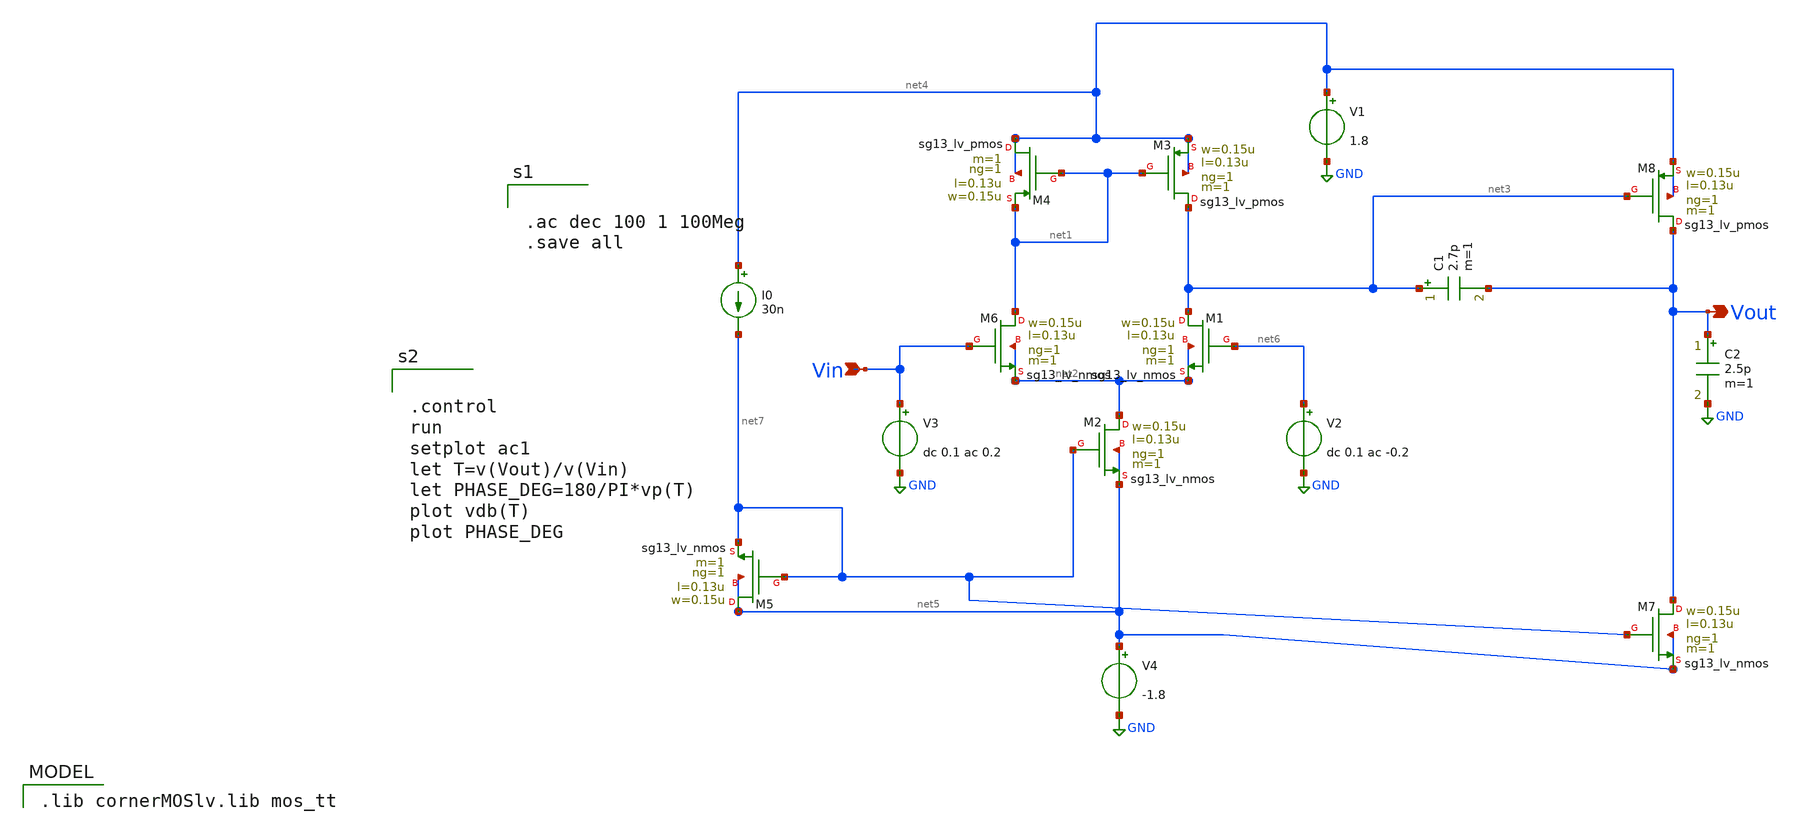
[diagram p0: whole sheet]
** sch_path: twostage.sch
* (c) 2024-2025 H. Pretl, Apache-2.0 license
**.subckt twostage Vout Vin
*.opin Vout
*.ipin Vin
V1 net4 GND 1.8
XM6 net1 Vin net2 net2 sg13_lv_nmos w=0.15u l=0.13u ng=1 m=1 mm_ok=1
XM1 net3 net6 net2 net2 sg13_lv_nmos w=0.15u l=0.13u ng=1 m=1 mm_ok=1
XM2 net2 net7 net5 net5 sg13_lv_nmos w=0.15u l=0.13u ng=1 m=1 mm_ok=1
XM3 net3 net1 net4 net4 sg13_lv_pmos w=0.15u l=0.13u ng=1 m=1 mm_ok=1
XM4 net4 net1 net1 net4 sg13_lv_pmos w=0.15u l=0.13u ng=1 m=1 mm_ok=1
V2 net6 GND dc 0.1 ac -0.2
V3 Vin GND dc 0.1 ac 0.2
V4 net5 GND -1.8
I0 net4 net7 30n
XM5 net5 net7 net7 net5 sg13_lv_nmos w=0.15u l=0.13u ng=1 m=1 mm_ok=1
XM7 Vout net7 net5 net5 sg13_lv_nmos w=0.15u l=0.13u ng=1 m=1 mm_ok=1
XM8 Vout net3 net4 net4 sg13_lv_pmos w=0.15u l=0.13u ng=1 m=1 mm_ok=1
C1 net3 Vout 2.7p m=1
C2 Vout GND 2.5p m=1
**** begin user architecture code
 .lib cornerMOSlv.lib mos_tt



.ac dec 100 1 100Meg
.save all




.control
run
setplot ac1
let T=v(Vout)/v(Vin)
let PHASE_DEG=180/PI*vp(T)
plot vdb(T)
plot PHASE_DEG


**** end user architecture code
**.ends
.GLOBAL GND
.end
